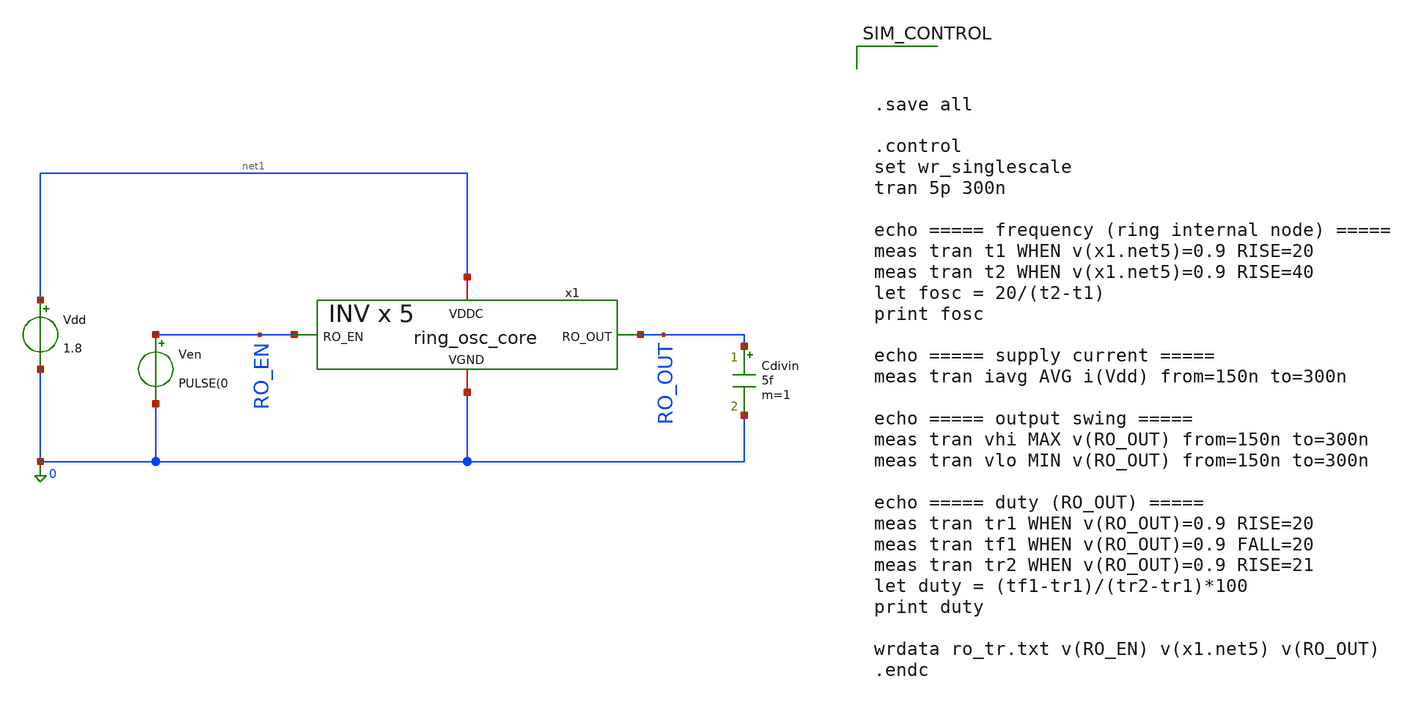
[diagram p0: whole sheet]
** sch_path: designs/bgr_ldo/ldo/ring_osc_tb.sch
**.subckt ring_osc_tb
x1 net1 RO_EN 0 RO_OUT ring_osc_core
Vdd net1 0 1.8
Ven RO_EN 0 PULSE(0
Cdivin RO_OUT 0 5f m=1
**** begin user architecture code

** opencircuitdesign pdks install
.lib $::SKYWATER_MODELS/sky130.lib.spice tt




.save all

.control
set wr_singlescale
tran 5p 300n

echo ===== frequency (ring internal node) =====
meas tran t1 WHEN v(x1.net5)=0.9 RISE=20
meas tran t2 WHEN v(x1.net5)=0.9 RISE=40
let fosc = 20/(t2-t1)
print fosc

echo ===== supply current =====
meas tran iavg AVG i(Vdd) from=150n to=300n

echo ===== output swing =====
meas tran vhi MAX v(RO_OUT) from=150n to=300n
meas tran vlo MIN v(RO_OUT) from=150n to=300n

echo ===== duty (RO_OUT) =====
meas tran tr1 WHEN v(RO_OUT)=0.9 RISE=20
meas tran tf1 WHEN v(RO_OUT)=0.9 FALL=20
meas tran tr2 WHEN v(RO_OUT)=0.9 RISE=21
let duty = (tf1-tr1)/(tr2-tr1)*100
print duty

wrdata ro_tr.txt v(RO_EN) v(x1.net5) v(RO_OUT)
.endc



**** end user architecture code
**.ends

* expanding   symbol:  ring_osc_core.sym # of pins=4
** sym_path: designs/bgr_ldo/ldo/ring_osc_core.sym
** sch_path: designs/bgr_ldo/ldo/ring_osc_core.sch
.subckt ring_osc_core VDDC RO_EN VGND RO_OUT
*.iopin VDDC
*.iopin VGND
*.opin RO_OUT
*.ipin RO_EN
x1 VDDC net5 net1 VGND ro_inv
x0 VDDC net4 RO_EN net5 VGND ro_nand
XC1 net1 VGND sky130_fd_pr__cap_mim_m3_1 W=4.27 L=4.27 MF=1 m=1
x2 VDDC net1 net2 VGND ro_inv
XC2 net2 VGND sky130_fd_pr__cap_mim_m3_1 W=4.27 L=4.27 MF=1 m=1
x3 VDDC net2 net3 VGND ro_inv
XC3 net3 VGND sky130_fd_pr__cap_mim_m3_1 W=4.27 L=4.27 MF=1 m=1
XC4 net4 VGND sky130_fd_pr__cap_mim_m3_1 W=4.27 L=4.27 MF=1 m=1
xB1 VDDC net4 net6 VGND ro_inv
xB2 VDDC net6 RO_OUT VGND ro_inv
XC5 net5 VGND sky130_fd_pr__cap_mim_m3_1 W=4.27 L=4.27 MF=1 m=1
x4 VDDC net3 net4 VGND ro_inv
.ends


* expanding   symbol:  ro_inv.sym # of pins=4
** sym_path: designs/bgr_ldo/ldo/ro_inv.sym
** sch_path: designs/bgr_ldo/ldo/ro_inv.sch
.subckt ro_inv VDDC A Y VGND
*.iopin VDDC
*.iopin VGND
*.ipin A
*.opin Y
XMP Y A VDDC VDDC sky130_fd_pr__pfet_01v8 L=0.15 W=1 nf=1 ad='int((1 + 1)/2) * 1 / 1 * 0.29' as='int((1 + 2)/2) * 1 / 1 * 0.29'
+ pd='2*int((1 + 1)/2) * (1 / 1 + 0.29)' ps='2*int((1 + 2)/2) * (1 / 1 + 0.29)' nrd='0.29 / 1 ' nrs='0.29 / 1 '
+ sa=0 sb=0 sd=0 mult=1 m=1
XMN Y A VGND VGND sky130_fd_pr__nfet_01v8 L=0.15 W=0.42 nf=1 ad='int((1 + 1)/2) * 0.42 / 1 * 0.29' as='int((1 + 2)/2) * 0.42 / 1 * 0.29'
+ pd='2*int((1 + 1)/2) * (0.42 / 1 + 0.29)' ps='2*int((1 + 2)/2) * (0.42 / 1 + 0.29)' nrd='0.29 / 0.42 '
+ nrs='0.29 / 0.42 ' sa=0 sb=0 sd=0 mult=1 m=1
.ends


* expanding   symbol:  ro_nand.sym # of pins=5
** sym_path: designs/bgr_ldo/ldo/ro_nand.sym
** sch_path: designs/bgr_ldo/ldo/ro_nand.sch
.subckt ro_nand VDDC A B Y VGND
*.iopin VDDC
*.iopin VGND
*.ipin A
*.opin Y
*.ipin B
XMP1 Y B VDDC VDDC sky130_fd_pr__pfet_01v8 L=0.15 W=1 nf=1 ad='int((1 + 1)/2) * 1 / 1 * 0.29' as='int((1 + 2)/2) * 1 / 1 * 0.29'
+ pd='2*int((1 + 1)/2) * (1 / 1 + 0.29)' ps='2*int((1 + 2)/2) * (1 / 1 + 0.29)' nrd='0.29 / 1 ' nrs='0.29 / 1 '
+ sa=0 sb=0 sd=0 mult=1 m=1
XMP2 Y A VDDC VDDC sky130_fd_pr__pfet_01v8 L=0.15 W=1 nf=1 ad='int((1 + 1)/2) * 1 / 1 * 0.29' as='int((1 + 2)/2) * 1 / 1 * 0.29'
+ pd='2*int((1 + 1)/2) * (1 / 1 + 0.29)' ps='2*int((1 + 2)/2) * (1 / 1 + 0.29)' nrd='0.29 / 1 ' nrs='0.29 / 1 '
+ sa=0 sb=0 sd=0 mult=1 m=1
XMN1 Y A n_nandmid VGND sky130_fd_pr__nfet_01v8 L=0.15 W=1 nf=1 ad='int((1 + 1)/2) * 1 / 1 * 0.29' as='int((1 + 2)/2) * 1 / 1 * 0.29'
+ pd='2*int((1 + 1)/2) * (1 / 1 + 0.29)' ps='2*int((1 + 2)/2) * (1 / 1 + 0.29)' nrd='0.29 / 1 ' nrs='0.29 / 1 '
+ sa=0 sb=0 sd=0 mult=1 m=1
XMN2 n_nandmid B VGND VGND sky130_fd_pr__nfet_01v8 L=0.15 W=1 nf=1 ad='int((1 + 1)/2) * 1 / 1 * 0.29'
+ as='int((1 + 2)/2) * 1 / 1 * 0.29' pd='2*int((1 + 1)/2) * (1 / 1 + 0.29)' ps='2*int((1 + 2)/2) * (1 / 1 + 0.29)'
+ nrd='0.29 / 1 ' nrs='0.29 / 1 ' sa=0 sb=0 sd=0 mult=1 m=1
.ends

.end
